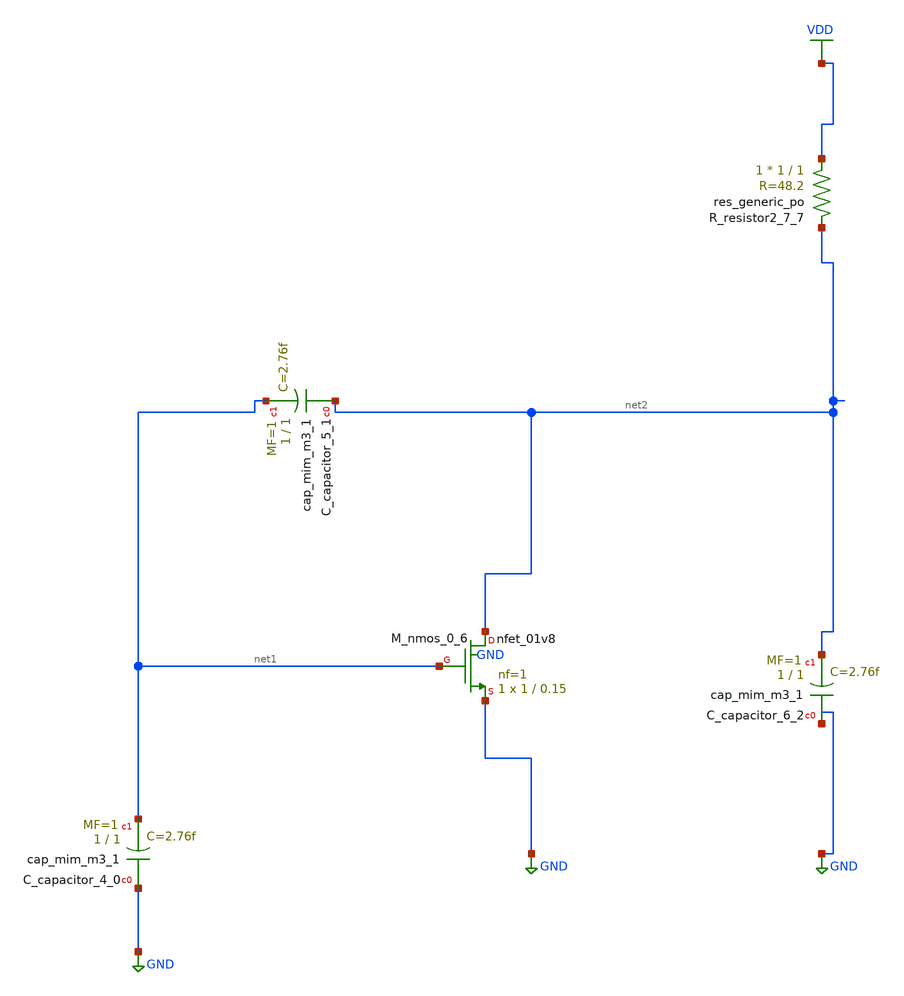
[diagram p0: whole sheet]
** sch_path: schematics/AMSNet/363.sch
**.subckt 363
XC_capacitor_4_0 GND net1 sky130_fd_pr__cap_mim_m3_1 W=1 L=1 MF=1 m=1
XC_capacitor_5_1 net2 net1 sky130_fd_pr__cap_mim_m3_1 W=1 L=1 MF=1 m=1
XC_capacitor_6_2 GND net2 sky130_fd_pr__cap_mim_m3_1 W=1 L=1 MF=1 m=1
XM_nmos_0_6 net2 net1 GND GND sky130_fd_pr__nfet_01v8 L=0.15 W=1 nf=1 ad='int((1 + 1)/2) * 1 / 1 * 0.29'
+ as='int((1 + 2)/2) * 1 / 1 * 0.29' pd='2*int((1 + 1)/2) * (1 / 1 + 0.29)' ps='2*int((1 + 2)/2) * (1 / 1 + 0.29)'
+ nrd='0.29 / 1 ' nrs='0.29 / 1 ' sa=0 sb=0 sd=0 mult=1 m=1
XR_resistor2_7_7 VDD net2 sky130_fd_pr__res_generic_po W=1 L=1 m=1
**.ends
.GLOBAL GND
.GLOBAL VDD
.end
